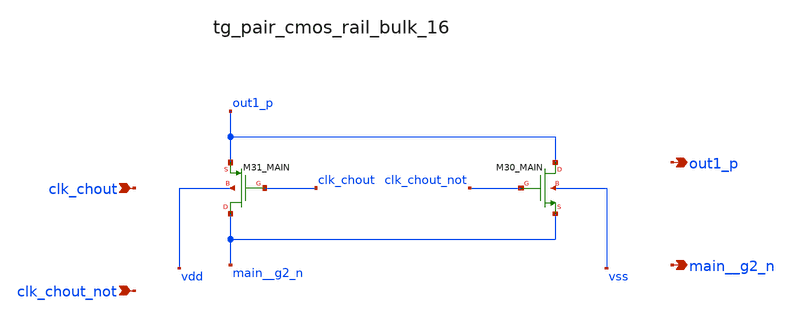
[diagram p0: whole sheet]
** sch_path: analog-db/raw/ia_004_fan_chopper_rrl/hier/blocks/tg_pair_cmos_rail_bulk_16.sch
**.subckt tg_pair_cmos_rail_bulk_16 clk_chout clk_chout_not out1_p main__g2_n
*.ipin clk_chout
*.ipin clk_chout_not
*.opin out1_p
*.opin main__g2_n
XM30_MAIN out1_p clk_chout_not main__g2_n vss sg13_lv_nmos w=x_dut_xm30_main_w l=x_dut_xm30_main_l
+ ng=1 m=x_dut_xm30_main_m
XM31_MAIN main__g2_n clk_chout out1_p vdd sg13_lv_pmos w=x_dut_xm31_main_w l=x_dut_xm31_main_l ng=1
+ m=x_dut_xm31_main_m
**.ends
.end
